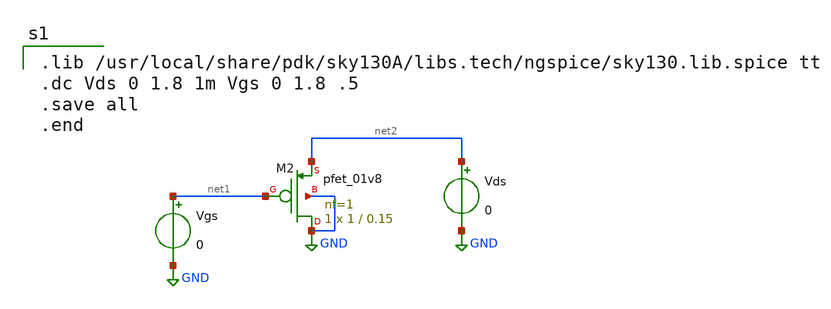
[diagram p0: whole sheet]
** sch_path: pmos_vtc.sch
**.subckt pmos_vtc
XM2 GND net1 net2 GND sky130_fd_pr__pfet_01v8 L=0.15 W=1 nf=1 ad='int((nf+1)/2) * W/nf * 0.29' as='int((nf+2)/2) * W/nf * 0.29'
+ pd='2*int((nf+1)/2) * (W/nf + 0.29)' ps='2*int((nf+2)/2) * (W/nf + 0.29)' nrd='0.29 / W' nrs='0.29 / W'
+ sa=0 sb=0 sd=0 mult=1 m=1
Vds net2 GND 0
Vgs net1 GND 0
**** begin user architecture code

.lib /usr/local/share/pdk/sky130A/libs.tech/ngspice/sky130.lib.spice tt
.dc Vds 0 1.8 1m Vgs 0 1.8 .5
.save all
.end

**** end user architecture code
**.ends
.GLOBAL GND
.end
